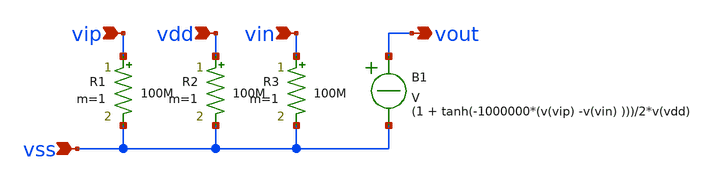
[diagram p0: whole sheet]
** sch_path: design/JNW_AVV_SKY130A/OTA.sch
**.subckt OTA vss vdd vin vip vout
*.ipin vss
*.ipin vdd
*.ipin vin
*.ipin vip
*.opin vout
B1 vout vss V = (1 + tanh(-1000000*(v(vip) -v(vin) )))/2*v(vdd)
R1 vip vss 100M m=1
R2 vdd vss 100M m=1
R3 vin vss 100M m=1
**.ends
.end
